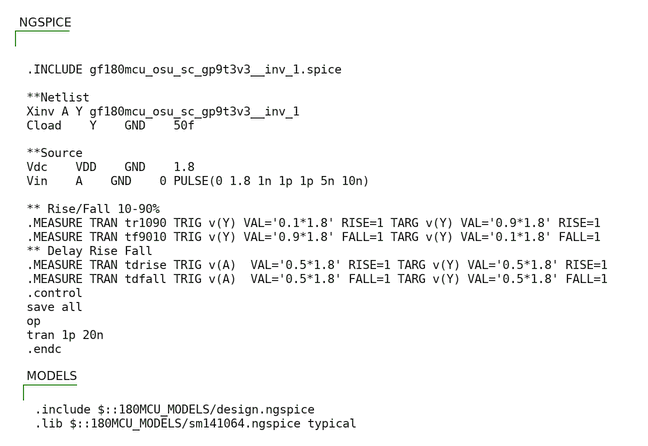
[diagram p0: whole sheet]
** sch_path: designs/libs/core_digital/gf180mcu_osu_sc_gp12t3v3/cells/and3/xschem/TB_inv.sch
**.subckt TB_inv
**** begin user architecture code

.include $::180MCU_MODELS/design.ngspice
.lib $::180MCU_MODELS/sm141064.ngspice typical




.INCLUDE gf180mcu_osu_sc_gp9t3v3__inv_1.spice

**Netlist
Xinv A Y gf180mcu_osu_sc_gp9t3v3__inv_1
Cload	Y	GND	50f

**Source
Vdc	VDD	GND	1.8
Vin	A	GND	0 PULSE(0 1.8 1n 1p 1p 5n 10n)

** Rise/Fall 10-90%
.MEASURE TRAN tr1090 TRIG v(Y) VAL='0.1*1.8' RISE=1 TARG v(Y) VAL='0.9*1.8' RISE=1
.MEASURE TRAN tf9010 TRIG v(Y) VAL='0.9*1.8' FALL=1 TARG v(Y) VAL='0.1*1.8' FALL=1
** Delay Rise Fall
.MEASURE TRAN tdrise TRIG v(A)  VAL='0.5*1.8' RISE=1 TARG v(Y) VAL='0.5*1.8' RISE=1
.MEASURE TRAN tdfall TRIG v(A)  VAL='0.5*1.8' FALL=1 TARG v(Y) VAL='0.5*1.8' FALL=1
.control
save all
op
tran 1p 20n
.endc


**** end user architecture code
**.ends
.end
